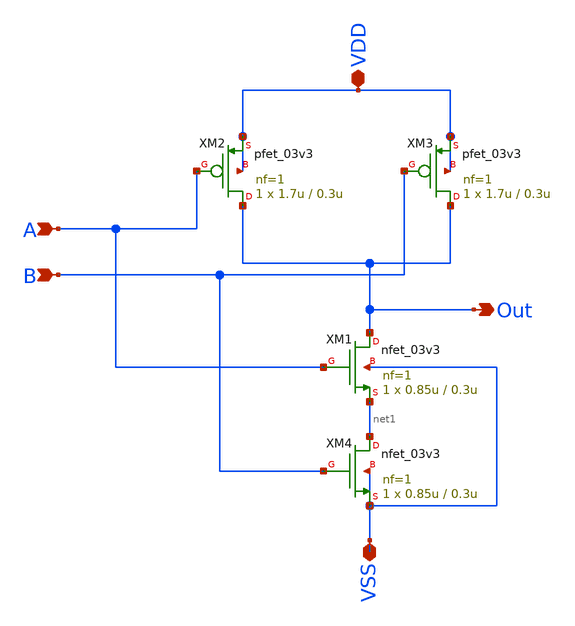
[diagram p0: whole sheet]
** sch_path: cells/comp4/comp4_2x/schematic/my_nand.sch
**.subckt my_nand A Out B VDD VSS
*.ipin A
*.opin Out
*.ipin B
*.iopin VDD
*.iopin VSS
XM1 Out A net1 VSS nfet_03v3 L=0.3u W=0.85u nf=1 ad='int((nf+1)/2) * W/nf * 0.18u' as='int((nf+2)/2) * W/nf * 0.18u'
+ pd='2*int((nf+1)/2) * (W/nf + 0.18u)' ps='2*int((nf+2)/2) * (W/nf + 0.18u)' nrd='0.18u / W' nrs='0.18u / W'
+ sa=0 sb=0 sd=0 m=1
XM2 Out A VDD VDD pfet_03v3 L=0.3u W=1.7u nf=1 ad='int((nf+1)/2) * W/nf * 0.18u' as='int((nf+2)/2) * W/nf * 0.18u'
+ pd='2*int((nf+1)/2) * (W/nf + 0.18u)' ps='2*int((nf+2)/2) * (W/nf + 0.18u)' nrd='0.18u / W' nrs='0.18u / W'
+ sa=0 sb=0 sd=0 m=1
XM3 Out B VDD VDD pfet_03v3 L=0.3u W=1.7u nf=1 ad='int((nf+1)/2) * W/nf * 0.18u' as='int((nf+2)/2) * W/nf * 0.18u'
+ pd='2*int((nf+1)/2) * (W/nf + 0.18u)' ps='2*int((nf+2)/2) * (W/nf + 0.18u)' nrd='0.18u / W' nrs='0.18u / W'
+ sa=0 sb=0 sd=0 m=1
XM4 net1 B VSS VSS nfet_03v3 L=0.3u W=0.85u nf=1 ad='int((nf+1)/2) * W/nf * 0.18u' as='int((nf+2)/2) * W/nf * 0.18u'
+ pd='2*int((nf+1)/2) * (W/nf + 0.18u)' ps='2*int((nf+2)/2) * (W/nf + 0.18u)' nrd='0.18u / W' nrs='0.18u / W'
+ sa=0 sb=0 sd=0 m=1
**.ends
.end
